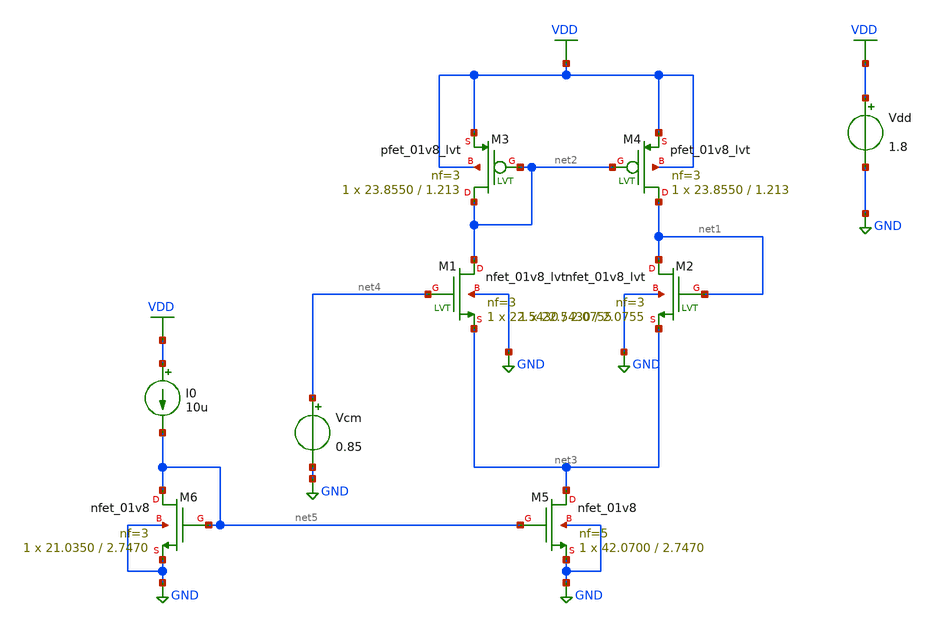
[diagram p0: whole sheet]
** sch_path: part2-full-spec-icmr-cmrr/cir/part2_OTA_advacned_ICMR.sch
**.subckt part2_OTA_advacned_ICMR
Vdd VDD GND 1.8
Vcm net4 GND 0.85
I0 VDD net5 10u
XM5 net3 net5 GND GND sky130_fd_pr__nfet_01v8 L=2.7470 W=42.0700 nf=5 ad='int((5 + 1)/2) * 42.0700 / 5 * 0.29'
+ as='int((5 + 2)/2) * 42.0700 / 5 * 0.29' pd='2*int((5 + 1)/2) * (42.0700 / 5 + 0.29)' ps='2*int((5 + 2)/2) * (42.0700 / 5 + 0.29)'
+ nrd='0.29 / 42.0700 ' nrs='0.29 / 42.0700 ' sa=0 sb=0 sd=0 mult=1 m=1
XM4 net1 net2 VDD VDD sky130_fd_pr__pfet_01v8_lvt L=1.213 W=23.8550 nf=3 ad='int((3 + 1)/2) * 23.8550 / 3 * 0.29'
+ as='int((3 + 2)/2) * 23.8550 / 3 * 0.29' pd='2*int((3 + 1)/2) * (23.8550 / 3 + 0.29)' ps='2*int((3 + 2)/2) * (23.8550 / 3 + 0.29)'
+ nrd='0.29 / 23.8550 ' nrs='0.29 / 23.8550 ' sa=0 sb=0 sd=0 mult=1 m=1
XM3 net2 net2 VDD VDD sky130_fd_pr__pfet_01v8_lvt L=1.213 W=23.8550 nf=3 ad='int((3 + 1)/2) * 23.8550 / 3 * 0.29'
+ as='int((3 + 2)/2) * 23.8550 / 3 * 0.29' pd='2*int((3 + 1)/2) * (23.8550 / 3 + 0.29)' ps='2*int((3 + 2)/2) * (23.8550 / 3 + 0.29)'
+ nrd='0.29 / 23.8550 ' nrs='0.29 / 23.8550 ' sa=0 sb=0 sd=0 mult=1 m=1
XM6 net5 net5 GND GND sky130_fd_pr__nfet_01v8 L=2.7470 W=21.0350 nf=3 ad='int((3 + 1)/2) * 21.0350 / 3 * 0.29'
+ as='int((3 + 2)/2) * 21.0350 / 3 * 0.29' pd='2*int((3 + 1)/2) * (21.0350 / 3 + 0.29)' ps='2*int((3 + 2)/2) * (21.0350 / 3 + 0.29)'
+ nrd='0.29 / 21.0350 ' nrs='0.29 / 21.0350 ' sa=0 sb=0 sd=0 mult=1 m=1
XM1 net2 net4 net3 GND sky130_fd_pr__nfet_01v8_lvt L=2.0755 W=22.5430 nf=3 ad='int((3 + 1)/2) * 22.5430 / 3 * 0.29'
+ as='int((3 + 2)/2) * 22.5430 / 3 * 0.29' pd='2*int((3 + 1)/2) * (22.5430 / 3 + 0.29)' ps='2*int((3 + 2)/2) * (22.5430 / 3 + 0.29)'
+ nrd='0.29 / 22.5430 ' nrs='0.29 / 22.5430 ' sa=0 sb=0 sd=0 mult=1 m=1
XM2 net1 net1 net3 GND sky130_fd_pr__nfet_01v8_lvt L=2.0755 W=22.5430 nf=3 ad='int((3 + 1)/2) * 22.5430 / 3 * 0.29'
+ as='int((3 + 2)/2) * 22.5430 / 3 * 0.29' pd='2*int((3 + 1)/2) * (22.5430 / 3 + 0.29)' ps='2*int((3 + 2)/2) * (22.5430 / 3 + 0.29)'
+ nrd='0.29 / 22.5430 ' nrs='0.29 / 22.5430 ' sa=0 sb=0 sd=0 mult=1 m=1
**** begin user architecture code


.lib /foss/pdks/sky130A/libs.tech/ngspice/sky130.lib.spice tt



.control


	save all

	* - Sweep Vcm
	dc Vcm 0 1.8 0.001

	* Get Vdiff
	let vdiff = v(net1) - v(net4)

	plot v(net1) v(net4) title 'ICMR Transfer Characteristic'
	plot vdiff title 'Tracking Deviation Error'

	meas dc vicm_min find v(net1) when vdiff=0.010 fall=1
	meas dc vicm_max find v(net1) when vdiff=-0.010 fall=1

.endc


**** end user architecture code
**.ends
.GLOBAL GND
.GLOBAL VDD
.end
